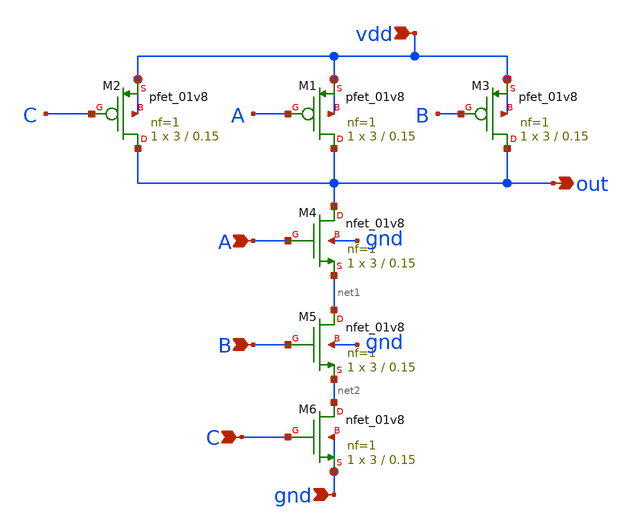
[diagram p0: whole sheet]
** sch_path: pll/dividers_lib/divider_init/xschem/nand_3in.sch
**.subckt nand_3in vdd A B gnd out C
*.ipin vdd
*.ipin A
*.ipin B
*.ipin gnd
*.opin out
*.ipin C
XM1 out A vdd vdd sky130_fd_pr__pfet_01v8 L=0.15 W=3 nf=1 ad='int((nf+1)/2) * W/nf * 0.29' as='int((nf+2)/2) * W/nf * 0.29'
+ pd='2*int((nf+1)/2) * (W/nf + 0.29)' ps='2*int((nf+2)/2) * (W/nf + 0.29)' nrd='0.29 / W' nrs='0.29 / W'
+ sa=0 sb=0 sd=0 mult=1 m=1
XM3 out B vdd vdd sky130_fd_pr__pfet_01v8 L=0.15 W=3 nf=1 ad='int((nf+1)/2) * W/nf * 0.29' as='int((nf+2)/2) * W/nf * 0.29'
+ pd='2*int((nf+1)/2) * (W/nf + 0.29)' ps='2*int((nf+2)/2) * (W/nf + 0.29)' nrd='0.29 / W' nrs='0.29 / W'
+ sa=0 sb=0 sd=0 mult=1 m=1
XM4 out A net1 gnd sky130_fd_pr__nfet_01v8 L=0.15 W=3 nf=1 ad='int((1 + 1)/2) * 3 / 1 * 0.29' as='int((1 + 2)/2) * 3 / 1 * 0.29'
+ pd='2*int((1 + 1)/2) * (3 / 1 + 0.29)' ps='2*int((1 + 2)/2) * (3 / 1 + 0.29)' nrd='0.29 / 3 ' nrs='0.29 / 3 '
+ sa=0 sb=0 sd=0 mult=1 m=1
XM5 net1 B net2 gnd sky130_fd_pr__nfet_01v8 L=0.15 W=3 nf=1 ad='int((1 + 1)/2) * 3 / 1 * 0.29' as='int((1 + 2)/2) * 3 / 1 * 0.29'
+ pd='2*int((1 + 1)/2) * (3 / 1 + 0.29)' ps='2*int((1 + 2)/2) * (3 / 1 + 0.29)' nrd='0.29 / 3 ' nrs='0.29 / 3 '
+ sa=0 sb=0 sd=0 mult=1 m=1
XM2 out C vdd vdd sky130_fd_pr__pfet_01v8 L=0.15 W=3 nf=1 ad='int((nf+1)/2) * W/nf * 0.29' as='int((nf+2)/2) * W/nf * 0.29'
+ pd='2*int((nf+1)/2) * (W/nf + 0.29)' ps='2*int((nf+2)/2) * (W/nf + 0.29)' nrd='0.29 / W' nrs='0.29 / W'
+ sa=0 sb=0 sd=0 mult=1 m=1
XM6 net2 C gnd gnd sky130_fd_pr__nfet_01v8 L=0.15 W=3 nf=1 ad='int((1 + 1)/2) * 3 / 1 * 0.29' as='int((1 + 2)/2) * 3 / 1 * 0.29'
+ pd='2*int((1 + 1)/2) * (3 / 1 + 0.29)' ps='2*int((1 + 2)/2) * (3 / 1 + 0.29)' nrd='0.29 / 3 ' nrs='0.29 / 3 '
+ sa=0 sb=0 sd=0 mult=1 m=1
**.ends
.end
